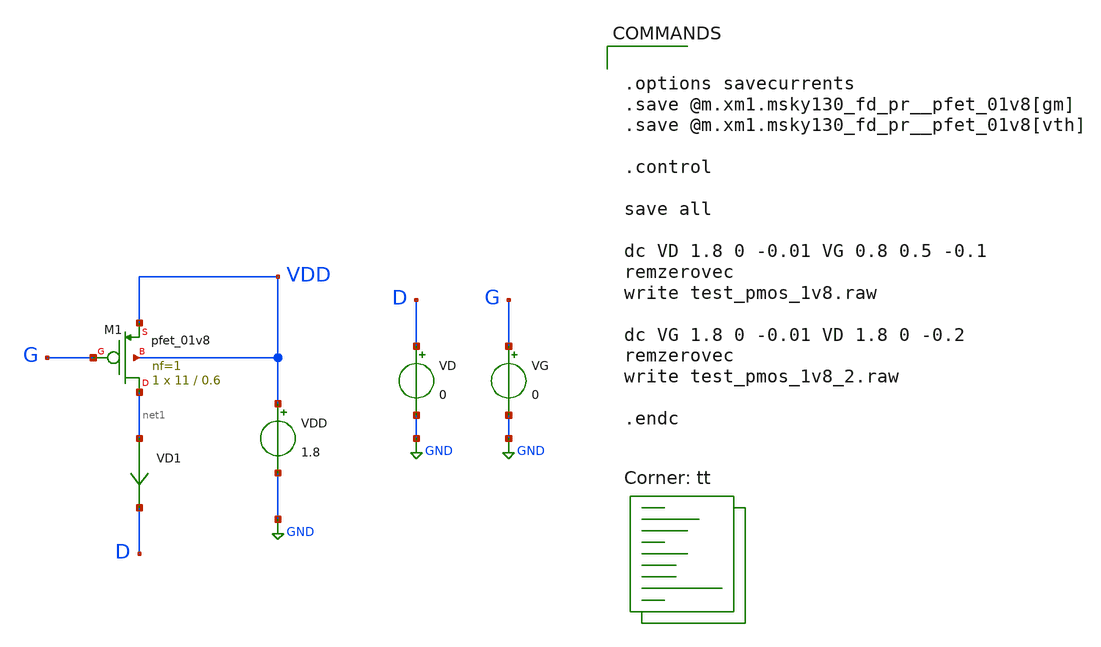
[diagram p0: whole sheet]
** sch_path: strongARM/test_pmos_1v8.sch
**.subckt test_pmos_1v8
VG G GND 0
VDD VDD GND 1.8
VD1 net1 D 0
.save i(vd1)
VD D GND 0
XM1 net1 G VDD VDD sky130_fd_pr__pfet_01v8 L=0.6 W=11 nf=1 ad='int((nf+1)/2) * W/nf * 0.29' as='int((nf+2)/2) * W/nf * 0.29'
+ pd='2*int((nf+1)/2) * (W/nf + 0.29)' ps='2*int((nf+2)/2) * (W/nf + 0.29)' nrd='0.29 / W' nrs='0.29 / W'
+ sa=0 sb=0 sd=0 mult=1 m=1
**** begin user architecture code
.lib $::SKYWATER_MODELS/sky130.lib.spice tt


.options savecurrents
.save @m.xm1.msky130_fd_pr__pfet_01v8[gm]
.save @m.xm1.msky130_fd_pr__pfet_01v8[vth]

.control

save all

dc VD 1.8 0 -0.01 VG 0.8 0.5 -0.1
remzerovec
write test_pmos_1v8.raw

dc VG 1.8 0 -0.01 VD 1.8 0 -0.2
remzerovec
write test_pmos_1v8_2.raw

.endc


**** end user architecture code
**.ends
.GLOBAL GND
.end
